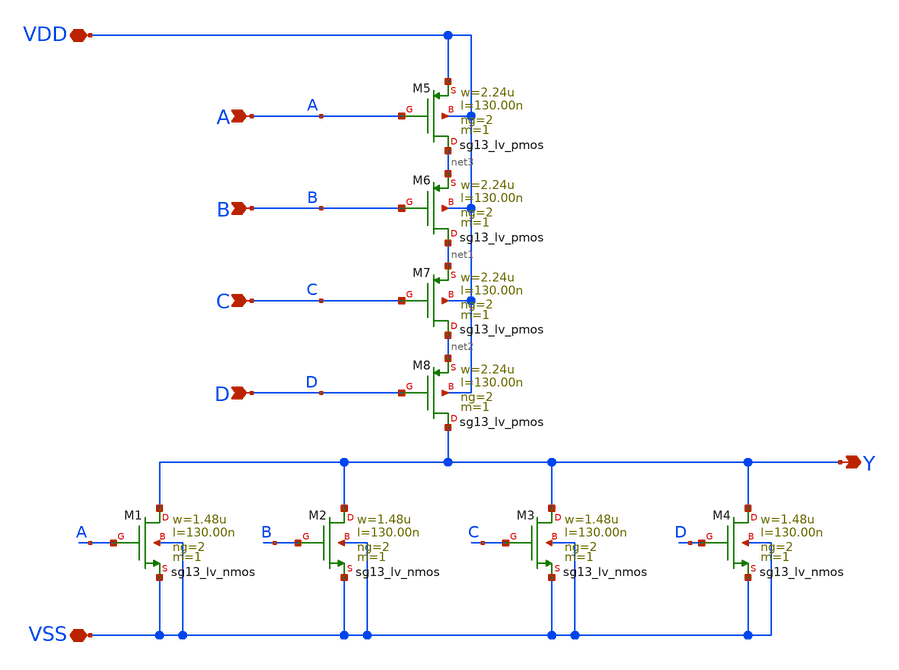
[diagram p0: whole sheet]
** sch_path: ihp-sg13g2/libs.tech/xschem/sg13g2_stdcells/sg13g2_nor4_2.sch
* Copyright 2023 IHP PDK Authors
* Licensed under the Apache License, Version 2.0 (the "License");
* you may not use this file except in compliance with the License.
* You may obtain a copy of the License at
* https://www.apache.org/licenses/LICENSE-2.0
* Unless required by applicable law or agreed to in writing, software
* distributed under the License is distributed on an "AS IS" BASIS,
* WITHOUT WARRANTIES OR CONDITIONS OF ANY KIND, either express or implied.
* See the License for the specific language governing permissions and
* limitations under the License.
**.subckt sg13g2_nor4_2 Y A B C D VDD VSS
*.opin Y
*.ipin A
*.ipin B
*.ipin C
*.ipin D
*.iopin VDD
*.iopin VSS
XM1 Y A VSS VSS sg13_lv_nmos w=1.48u l=130.00n ng=2 m=1 mm_ok=1
XM2 Y B VSS VSS sg13_lv_nmos w=1.48u l=130.00n ng=2 m=1 mm_ok=1
XM3 Y C VSS VSS sg13_lv_nmos w=1.48u l=130.00n ng=2 m=1 mm_ok=1
XM4 Y D VSS VSS sg13_lv_nmos w=1.48u l=130.00n ng=2 m=1 mm_ok=1
XM5 net3 A VDD VDD sg13_lv_pmos w=2.24u l=130.00n ng=2 m=1 mm_ok=1
XM6 net1 B net3 VDD sg13_lv_pmos w=2.24u l=130.00n ng=2 m=1 mm_ok=1
XM7 net2 C net1 VDD sg13_lv_pmos w=2.24u l=130.00n ng=2 m=1 mm_ok=1
XM8 Y D net2 VDD sg13_lv_pmos w=2.24u l=130.00n ng=2 m=1 mm_ok=1
**.ends
.end
